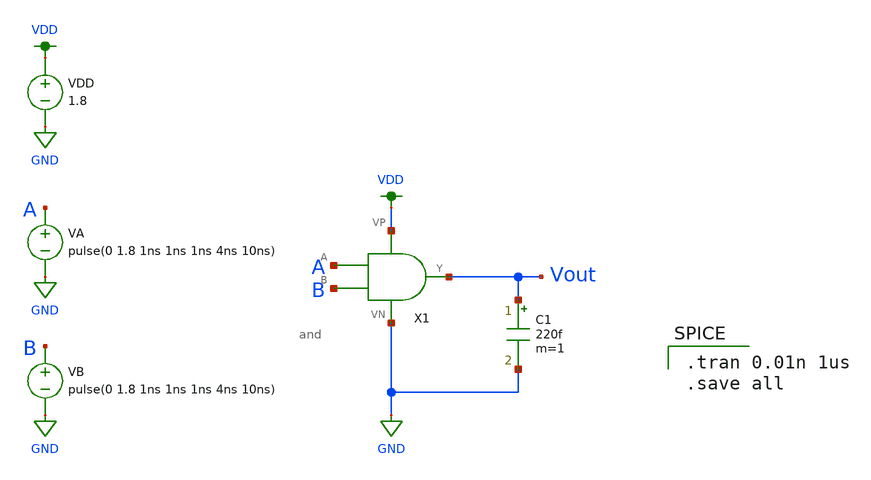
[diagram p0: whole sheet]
** sch_path: MP1/and_tran.sch
**.subckt and_tran
C1 Vout GND 220f m=1
VDD VDD GND 1.8
X1 A B Vout VDD GND and
VA A GND pulse(0 1.8 1ns 1ns 1ns 4ns 10ns)
VB B GND pulse(0 1.8 1ns 1ns 1ns 4ns 10ns)
**** begin user architecture code

.option wnflag=1
.lib ~/skywater/skywater-pdk/libraries/sky130_fd_pr_ngspice/latest/models/sky130.lib.spice tt


.tran 0.01n 1us
.save all

**** end user architecture code
**.ends

* expanding   symbol:  /home/madvlsi/Desktop/madvlsi/MP1/and.sym # of pins=5
** sym_path: MP1/and.sym
** sch_path: MP1/and.sch
.subckt and A B Y VP VN
*.ipin A
*.ipin B
*.iopin VP
*.iopin VN
*.opin Y
X1 net2 Y net3 net4 inverter
X2 B A VP VN net1 nand
.ends


* expanding   symbol:  /home/madvlsi/Desktop/madvlsi/MP1/inverter.sym # of pins=4
** sym_path: MP1/inverter.sym
** sch_path: MP1/inverter.sch
.subckt inverter A Y VP VN
*.ipin A
*.iopin VP
*.iopin VN
*.opin Y
XM1 Y A VP VP sky130_fd_pr__pfet_01v8 L=0.15 W=1 nf=1 ad='int((nf+1)/2) * W/nf * 0.29' as='int((nf+2)/2) * W/nf * 0.29'
+ pd='2*int((nf+1)/2) * (W/nf + 0.29)' ps='2*int((nf+2)/2) * (W/nf + 0.29)' nrd='0.29 / W' nrs='0.29 / W'
+ sa=0 sb=0 sd=0 mult=2 m=2
XM2 Y A VN VN sky130_fd_pr__nfet_01v8 L=0.15 W=1 nf=1 ad='int((nf+1)/2) * W/nf * 0.29' as='int((nf+2)/2) * W/nf * 0.29'
+ pd='2*int((nf+1)/2) * (W/nf + 0.29)' ps='2*int((nf+2)/2) * (W/nf + 0.29)' nrd='0.29 / W' nrs='0.29 / W'
+ sa=0 sb=0 sd=0 mult=1 m=1
.ends


* expanding   symbol:  /home/madvlsi/Desktop/madvlsi/MP1/nand.sym # of pins=5
** sym_path: MP1/nand.sym
** sch_path: MP1/nand.sch
.subckt nand B A VP VN Y
*.opin Y
*.iopin VP
*.iopin VN
*.ipin A
*.ipin B
*.iopin VN
XM1 Y A VP VP sky130_fd_pr__pfet_01v8 L=0.15 W=1 nf=1 ad='int((nf+1)/2) * W/nf * 0.29' as='int((nf+2)/2) * W/nf * 0.29'
+ pd='2*int((nf+1)/2) * (W/nf + 0.29)' ps='2*int((nf+2)/2) * (W/nf + 0.29)' nrd='0.29 / W' nrs='0.29 / W'
+ sa=0 sb=0 sd=0 mult=1 m=1
XM2 VP B Y VP sky130_fd_pr__pfet_01v8 L=0.15 W=1 nf=1 ad='int((nf+1)/2) * W/nf * 0.29' as='int((nf+2)/2) * W/nf * 0.29'
+ pd='2*int((nf+1)/2) * (W/nf + 0.29)' ps='2*int((nf+2)/2) * (W/nf + 0.29)' nrd='0.29 / W' nrs='0.29 / W'
+ sa=0 sb=0 sd=0 mult=1 m=1
XM3 Y A net1 VN sky130_fd_pr__nfet_01v8 L=0.15 W=1 nf=1 ad='int((nf+1)/2) * W/nf * 0.29' as='int((nf+2)/2) * W/nf * 0.29'
+ pd='2*int((nf+1)/2) * (W/nf + 0.29)' ps='2*int((nf+2)/2) * (W/nf + 0.29)' nrd='0.29 / W' nrs='0.29 / W'
+ sa=0 sb=0 sd=0 mult=1 m=1
XM4 VN B net1 VN sky130_fd_pr__nfet_01v8 L=0.15 W=1 nf=1 ad='int((nf+1)/2) * W/nf * 0.29' as='int((nf+2)/2) * W/nf * 0.29'
+ pd='2*int((nf+1)/2) * (W/nf + 0.29)' ps='2*int((nf+2)/2) * (W/nf + 0.29)' nrd='0.29 / W' nrs='0.29 / W'
+ sa=0 sb=0 sd=0 mult=1 m=1
.ends

.GLOBAL VDD
.GLOBAL GND
.end
